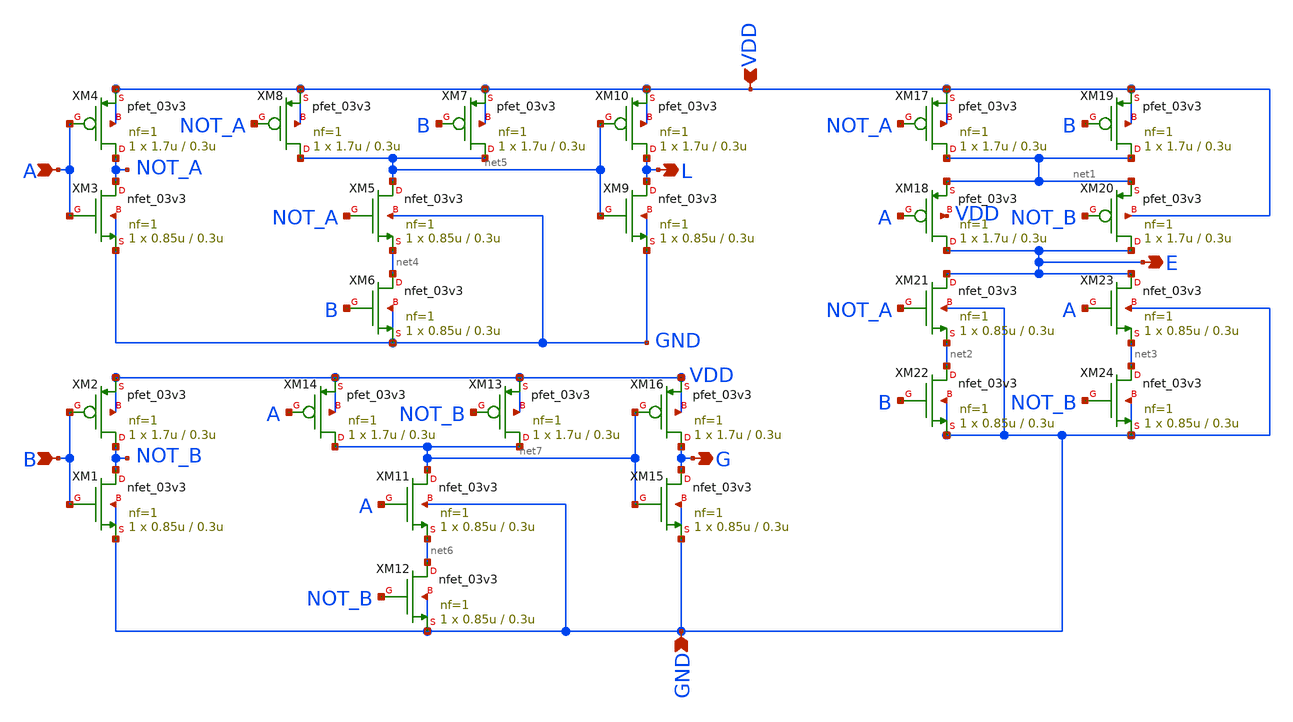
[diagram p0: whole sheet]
** sch_path: cell/comp2/xschem/comp2_1x.sch
**.subckt comp2_1x L G E A B VDD GND
*.opin L
*.opin G
*.opin E
*.ipin A
*.ipin B
*.ipin VDD
*.ipin GND
XM17 net1 NOT_A VDD VDD pfet_03v3 L=0.3u W=1.7u nf=1 ad='int((nf+1)/2) * W/nf * 0.18u' as='int((nf+2)/2) * W/nf * 0.18u'
+ pd='2*int((nf+1)/2) * (W/nf + 0.18u)' ps='2*int((nf+2)/2) * (W/nf + 0.18u)' nrd='0.18u / W' nrs='0.18u / W'
+ sa=0 sb=0 sd=0 m=1
XM18 E A net1 VDD pfet_03v3 L=0.3u W=1.7u nf=1 ad='int((nf+1)/2) * W/nf * 0.18u' as='int((nf+2)/2) * W/nf * 0.18u'
+ pd='2*int((nf+1)/2) * (W/nf + 0.18u)' ps='2*int((nf+2)/2) * (W/nf + 0.18u)' nrd='0.18u / W' nrs='0.18u / W'
+ sa=0 sb=0 sd=0 m=1
XM19 net1 B VDD VDD pfet_03v3 L=0.3u W=1.7u nf=1 ad='int((nf+1)/2) * W/nf * 0.18u' as='int((nf+2)/2) * W/nf * 0.18u'
+ pd='2*int((nf+1)/2) * (W/nf + 0.18u)' ps='2*int((nf+2)/2) * (W/nf + 0.18u)' nrd='0.18u / W' nrs='0.18u / W'
+ sa=0 sb=0 sd=0 m=1
XM20 E NOT_B net1 VDD pfet_03v3 L=0.3u W=1.7u nf=1 ad='int((nf+1)/2) * W/nf * 0.18u' as='int((nf+2)/2) * W/nf * 0.18u'
+ pd='2*int((nf+1)/2) * (W/nf + 0.18u)' ps='2*int((nf+2)/2) * (W/nf + 0.18u)' nrd='0.18u / W' nrs='0.18u / W'
+ sa=0 sb=0 sd=0 m=1
XM21 E NOT_A net2 GND nfet_03v3 L=0.3u W=0.85u nf=1 ad='int((nf+1)/2) * W/nf * 0.18u' as='int((nf+2)/2) * W/nf * 0.18u'
+ pd='2*int((nf+1)/2) * (W/nf + 0.18u)' ps='2*int((nf+2)/2) * (W/nf + 0.18u)' nrd='0.18u / W' nrs='0.18u / W'
+ sa=0 sb=0 sd=0 m=1
XM22 net2 B GND GND nfet_03v3 L=0.3u W=0.85u nf=1 ad='int((nf+1)/2) * W/nf * 0.18u' as='int((nf+2)/2) * W/nf * 0.18u'
+ pd='2*int((nf+1)/2) * (W/nf + 0.18u)' ps='2*int((nf+2)/2) * (W/nf + 0.18u)' nrd='0.18u / W' nrs='0.18u / W'
+ sa=0 sb=0 sd=0 m=1
XM23 E A net3 GND nfet_03v3 L=0.3u W=0.85u nf=1 ad='int((nf+1)/2) * W/nf * 0.18u' as='int((nf+2)/2) * W/nf * 0.18u'
+ pd='2*int((nf+1)/2) * (W/nf + 0.18u)' ps='2*int((nf+2)/2) * (W/nf + 0.18u)' nrd='0.18u / W' nrs='0.18u / W'
+ sa=0 sb=0 sd=0 m=1
XM24 net3 NOT_B GND GND nfet_03v3 L=0.3u W=0.85u nf=1 ad='int((nf+1)/2) * W/nf * 0.18u' as='int((nf+2)/2) * W/nf * 0.18u'
+ pd='2*int((nf+1)/2) * (W/nf + 0.18u)' ps='2*int((nf+2)/2) * (W/nf + 0.18u)' nrd='0.18u / W' nrs='0.18u / W'
+ sa=0 sb=0 sd=0 m=1
XM1 NOT_B B GND GND nfet_03v3 L=0.3u W=0.85u nf=1 ad='int((nf+1)/2) * W/nf * 0.18u' as='int((nf+2)/2) * W/nf * 0.18u'
+ pd='2*int((nf+1)/2) * (W/nf + 0.18u)' ps='2*int((nf+2)/2) * (W/nf + 0.18u)' nrd='0.18u / W' nrs='0.18u / W'
+ sa=0 sb=0 sd=0 m=1
XM2 NOT_B B VDD VDD pfet_03v3 L=0.3u W=1.7u nf=1 ad='int((nf+1)/2) * W/nf * 0.18u' as='int((nf+2)/2) * W/nf * 0.18u'
+ pd='2*int((nf+1)/2) * (W/nf + 0.18u)' ps='2*int((nf+2)/2) * (W/nf + 0.18u)' nrd='0.18u / W' nrs='0.18u / W'
+ sa=0 sb=0 sd=0 m=1
XM3 NOT_A A GND GND nfet_03v3 L=0.3u W=0.85u nf=1 ad='int((nf+1)/2) * W/nf * 0.18u' as='int((nf+2)/2) * W/nf * 0.18u'
+ pd='2*int((nf+1)/2) * (W/nf + 0.18u)' ps='2*int((nf+2)/2) * (W/nf + 0.18u)' nrd='0.18u / W' nrs='0.18u / W'
+ sa=0 sb=0 sd=0 m=1
XM4 NOT_A A VDD VDD pfet_03v3 L=0.3u W=1.7u nf=1 ad='int((nf+1)/2) * W/nf * 0.18u' as='int((nf+2)/2) * W/nf * 0.18u'
+ pd='2*int((nf+1)/2) * (W/nf + 0.18u)' ps='2*int((nf+2)/2) * (W/nf + 0.18u)' nrd='0.18u / W' nrs='0.18u / W'
+ sa=0 sb=0 sd=0 m=1
XM5 net5 NOT_A net4 GND nfet_03v3 L=0.3u W=0.85u nf=1 ad='int((nf+1)/2) * W/nf * 0.18u' as='int((nf+2)/2) * W/nf * 0.18u'
+ pd='2*int((nf+1)/2) * (W/nf + 0.18u)' ps='2*int((nf+2)/2) * (W/nf + 0.18u)' nrd='0.18u / W' nrs='0.18u / W'
+ sa=0 sb=0 sd=0 m=1
XM6 net4 B GND GND nfet_03v3 L=0.3u W=0.85u nf=1 ad='int((nf+1)/2) * W/nf * 0.18u' as='int((nf+2)/2) * W/nf * 0.18u'
+ pd='2*int((nf+1)/2) * (W/nf + 0.18u)' ps='2*int((nf+2)/2) * (W/nf + 0.18u)' nrd='0.18u / W' nrs='0.18u / W'
+ sa=0 sb=0 sd=0 m=1
XM7 net5 B VDD VDD pfet_03v3 L=0.3u W=1.7u nf=1 ad='int((nf+1)/2) * W/nf * 0.18u' as='int((nf+2)/2) * W/nf * 0.18u'
+ pd='2*int((nf+1)/2) * (W/nf + 0.18u)' ps='2*int((nf+2)/2) * (W/nf + 0.18u)' nrd='0.18u / W' nrs='0.18u / W'
+ sa=0 sb=0 sd=0 m=1
XM8 net5 NOT_A VDD VDD pfet_03v3 L=0.3u W=1.7u nf=1 ad='int((nf+1)/2) * W/nf * 0.18u' as='int((nf+2)/2) * W/nf * 0.18u'
+ pd='2*int((nf+1)/2) * (W/nf + 0.18u)' ps='2*int((nf+2)/2) * (W/nf + 0.18u)' nrd='0.18u / W' nrs='0.18u / W'
+ sa=0 sb=0 sd=0 m=1
XM9 L net5 GND GND nfet_03v3 L=0.3u W=0.85u nf=1 ad='int((nf+1)/2) * W/nf * 0.18u' as='int((nf+2)/2) * W/nf * 0.18u'
+ pd='2*int((nf+1)/2) * (W/nf + 0.18u)' ps='2*int((nf+2)/2) * (W/nf + 0.18u)' nrd='0.18u / W' nrs='0.18u / W'
+ sa=0 sb=0 sd=0 m=1
XM10 L net5 VDD VDD pfet_03v3 L=0.3u W=1.7u nf=1 ad='int((nf+1)/2) * W/nf * 0.18u' as='int((nf+2)/2) * W/nf * 0.18u'
+ pd='2*int((nf+1)/2) * (W/nf + 0.18u)' ps='2*int((nf+2)/2) * (W/nf + 0.18u)' nrd='0.18u / W' nrs='0.18u / W'
+ sa=0 sb=0 sd=0 m=1
XM11 net7 A net6 GND nfet_03v3 L=0.3u W=0.85u nf=1 ad='int((nf+1)/2) * W/nf * 0.18u' as='int((nf+2)/2) * W/nf * 0.18u'
+ pd='2*int((nf+1)/2) * (W/nf + 0.18u)' ps='2*int((nf+2)/2) * (W/nf + 0.18u)' nrd='0.18u / W' nrs='0.18u / W'
+ sa=0 sb=0 sd=0 m=1
XM12 net6 NOT_B GND GND nfet_03v3 L=0.3u W=0.85u nf=1 ad='int((nf+1)/2) * W/nf * 0.18u' as='int((nf+2)/2) * W/nf * 0.18u'
+ pd='2*int((nf+1)/2) * (W/nf + 0.18u)' ps='2*int((nf+2)/2) * (W/nf + 0.18u)' nrd='0.18u / W' nrs='0.18u / W'
+ sa=0 sb=0 sd=0 m=1
XM13 net7 NOT_B VDD VDD pfet_03v3 L=0.3u W=1.7u nf=1 ad='int((nf+1)/2) * W/nf * 0.18u' as='int((nf+2)/2) * W/nf * 0.18u'
+ pd='2*int((nf+1)/2) * (W/nf + 0.18u)' ps='2*int((nf+2)/2) * (W/nf + 0.18u)' nrd='0.18u / W' nrs='0.18u / W'
+ sa=0 sb=0 sd=0 m=1
XM14 net7 A VDD VDD pfet_03v3 L=0.3u W=1.7u nf=1 ad='int((nf+1)/2) * W/nf * 0.18u' as='int((nf+2)/2) * W/nf * 0.18u'
+ pd='2*int((nf+1)/2) * (W/nf + 0.18u)' ps='2*int((nf+2)/2) * (W/nf + 0.18u)' nrd='0.18u / W' nrs='0.18u / W'
+ sa=0 sb=0 sd=0 m=1
XM15 G net7 GND GND nfet_03v3 L=0.3u W=0.85u nf=1 ad='int((nf+1)/2) * W/nf * 0.18u' as='int((nf+2)/2) * W/nf * 0.18u'
+ pd='2*int((nf+1)/2) * (W/nf + 0.18u)' ps='2*int((nf+2)/2) * (W/nf + 0.18u)' nrd='0.18u / W' nrs='0.18u / W'
+ sa=0 sb=0 sd=0 m=1
XM16 G net7 VDD VDD pfet_03v3 L=0.3u W=1.7u nf=1 ad='int((nf+1)/2) * W/nf * 0.18u' as='int((nf+2)/2) * W/nf * 0.18u'
+ pd='2*int((nf+1)/2) * (W/nf + 0.18u)' ps='2*int((nf+2)/2) * (W/nf + 0.18u)' nrd='0.18u / W' nrs='0.18u / W'
+ sa=0 sb=0 sd=0 m=1
**.ends
.end
